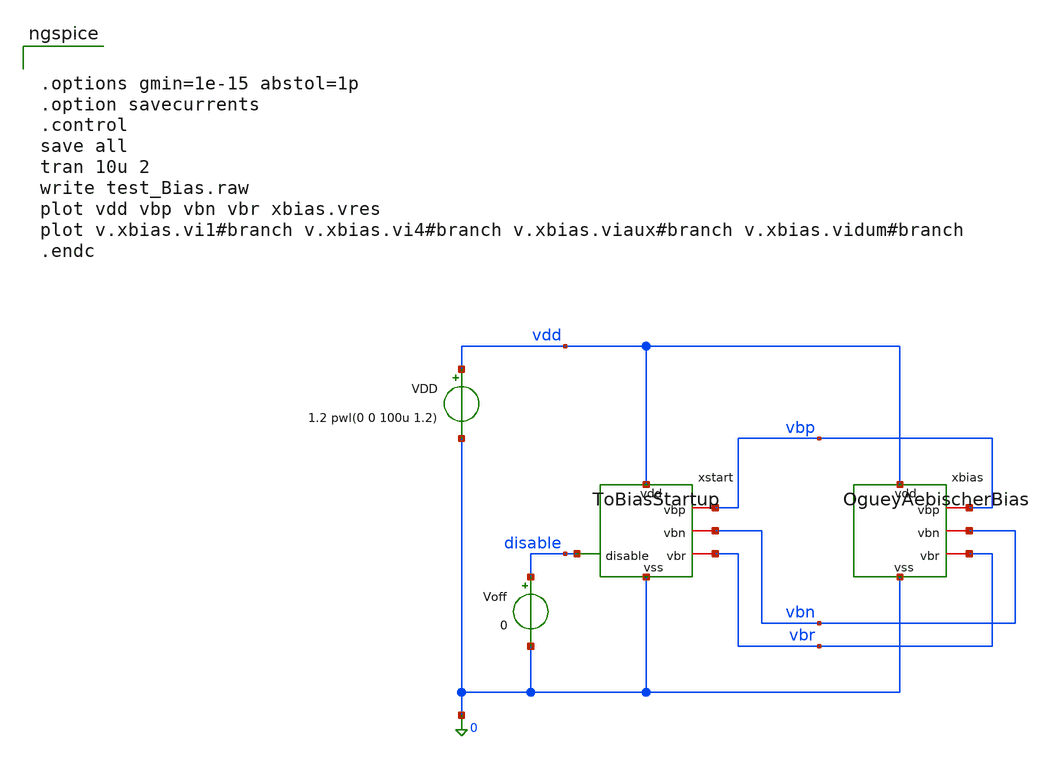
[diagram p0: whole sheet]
** sch_path: playground/test_Bias.sch
**.subckt test_Bias
xbias vdd vbp vbn vbr 0 OgueyAebischerBias
xstart vdd vbp vbn disable vbr 0 ToBiasStartup
VDD vdd 0 1.2 pwl(0 0 100u 1.2)
Voff disable 0 0
**** begin user architecture code


.options gmin=1e-15 abstol=1p
.option savecurrents
.control
save all
tran 10u 2
write test_Bias.raw
plot vdd vbp vbn vbr xbias.vres
plot v.xbias.vi1#branch v.xbias.vi4#branch v.xbias.viaux#branch v.xbias.vidum#branch
.endc


 .lib $::SKYWATER_MODELS/models/sky130.lib.spice tt

.param mc_mm_switch=0
.param mc_pr_switch=1


**** end user architecture code
**.ends

* expanding   symbol:  OgueyAebischerBias.sym # of pins=5
** sym_path: OgueyAebischerBias.sym
** sch_path: OgueyAebischerBias.sch
.subckt OgueyAebischerBias vdd vbp vbn vbr vss
*.iopin vss
*.iopin vdd
*.iopin vbp
*.iopin vbn
*.iopin vbr
XM10 net3 vbn vres vss sky130_fd_pr__nfet_01v8 L=10 W=1 nf=1 ad='int((1 + 1)/2) * 1 / 1 * 0.29' as='int((1 + 2)/2) * 1 / 1 * 0.29'
+ pd='2*int((1 + 1)/2) * (1 / 1 + 0.29)' ps='2*int((1 + 2)/2) * (1 / 1 + 0.29)' nrd='0.29 / 1 ' nrs='0.29 / 1 '
+ sa=0 sb=0 sd=0 mult=4 m=4
XM12 vbp vbp vdd vdd sky130_fd_pr__pfet_01v8 L=10 W=1 nf=1 ad='int((nf+1)/2) * W/nf * 0.29' as='int((nf+2)/2) * W/nf * 0.29'
+ pd='2*int((nf+1)/2) * (W/nf + 0.29)' ps='2*int((nf+2)/2) * (W/nf + 0.29)' nrd='0.29 / W' nrs='0.29 / W'
+ sa=0 sb=0 sd=0 mult=1 m=1
XM11 vbn vbn vss vss sky130_fd_pr__nfet_01v8 L=10 W=1 nf=1 ad='int((1 + 1)/2) * 1 / 1 * 0.29' as='int((1 + 2)/2) * 1 / 1 * 0.29'
+ pd='2*int((1 + 1)/2) * (1 / 1 + 0.29)' ps='2*int((1 + 2)/2) * (1 / 1 + 0.29)' nrd='0.29 / 1 ' nrs='0.29 / 1 '
+ sa=0 sb=0 sd=0 mult=1 m=1
XM13 net2 vbp vdd vdd sky130_fd_pr__pfet_01v8 L=10 W=1 nf=1 ad='int((nf+1)/2) * W/nf * 0.29' as='int((nf+2)/2) * W/nf * 0.29'
+ pd='2*int((nf+1)/2) * (W/nf + 0.29)' ps='2*int((nf+2)/2) * (W/nf + 0.29)' nrd='0.29 / W' nrs='0.29 / W'
+ sa=0 sb=0 sd=0 mult=4 m=4
XM14 net1 vbp vdd vdd sky130_fd_pr__pfet_01v8 L=10 W=1 nf=1 ad='int((nf+1)/2) * W/nf * 0.29' as='int((nf+2)/2) * W/nf * 0.29'
+ pd='2*int((nf+1)/2) * (W/nf + 0.29)' ps='2*int((nf+2)/2) * (W/nf + 0.29)' nrd='0.29 / W' nrs='0.29 / W'
+ sa=0 sb=0 sd=0 mult=1 m=1
XM16 net4 vbr vss vss sky130_fd_pr__nfet_01v8 L=80 W=0.5 nf=1 ad='int((1 + 1)/2) * 0.5 / 1 * 0.29' as='int((1 + 2)/2) * 0.5 / 1 * 0.29'
+ pd='2*int((1 + 1)/2) * (0.5 / 1 + 0.29)' ps='2*int((1 + 2)/2) * (0.5 / 1 + 0.29)' nrd='0.29 / 0.5 ' nrs='0.29 / 0.5 '
+ sa=0 sb=0 sd=0 mult=1 m=1
XM15 vbr vbr vss vss sky130_fd_pr__nfet_01v8 L=80 W=0.5 nf=1 ad='int((1 + 1)/2) * 0.5 / 1 * 0.29' as='int((1 + 2)/2) * 0.5 / 1 * 0.29'
+ pd='2*int((1 + 1)/2) * (0.5 / 1 + 0.29)' ps='2*int((1 + 2)/2) * (0.5 / 1 + 0.29)' nrd='0.29 / 0.5 ' nrs='0.29 / 0.5 '
+ sa=0 sb=0 sd=0 mult=1 m=1
Vi1 vbp net3 0
.save i(vi1)
Vi4 net2 vbn 0
.save i(vi4)
Viaux net1 vbr 0
.save i(viaux)
R1 vres vss 10000k m=1
Vidum net5 net4 0
.save i(vidum)
E1 vdd net5 vdd vres 1
.ends


* expanding   symbol:  ToBiasStartup.sym # of pins=6
** sym_path: ToBiasStartup.sym
** sch_path: ToBiasStartup.sch
.subckt ToBiasStartup vdd vbp vbn disable vbr vss
*.iopin vss
*.iopin vdd
*.iopin vbp
*.iopin vbn
*.iopin vbr
*.ipin disable
XM24 vbr disable vss vss sky130_fd_pr__nfet_01v8 L=0.3 W=1 nf=1 ad='int((1 + 1)/2) * 1 / 1 * 0.29' as='int((1 + 2)/2) * 1 / 1 * 0.29'
+ pd='2*int((1 + 1)/2) * (1 / 1 + 0.29)' ps='2*int((1 + 2)/2) * (1 / 1 + 0.29)' nrd='0.29 / 1 ' nrs='0.29 / 1 '
+ sa=0 sb=0 sd=0 mult=1 m=1
XM22 vbr vkick vdd vdd sky130_fd_pr__pfet_01v8 L=0.3 W=1 nf=1 ad='int((nf+1)/2) * W/nf * 0.29' as='int((nf+2)/2) * W/nf * 0.29'
+ pd='2*int((nf+1)/2) * (W/nf + 0.29)' ps='2*int((nf+2)/2) * (W/nf + 0.29)' nrd='0.29 / W' nrs='0.29 / W'
+ sa=0 sb=0 sd=0 mult=1 m=1
XM25 vkick vbp vdd vdd sky130_fd_pr__pfet_01v8 L=0.3 W=1 nf=1 ad='int((nf+1)/2) * W/nf * 0.29' as='int((nf+2)/2) * W/nf * 0.29'
+ pd='2*int((nf+1)/2) * (W/nf + 0.29)' ps='2*int((nf+2)/2) * (W/nf + 0.29)' nrd='0.29 / W' nrs='0.29 / W'
+ sa=0 sb=0 sd=0 mult=1 m=1
XM23 vbn disable vss vss sky130_fd_pr__nfet_01v8 L=0.3 W=1 nf=1 ad='int((1 + 1)/2) * 1 / 1 * 0.29' as='int((1 + 2)/2) * 1 / 1 * 0.29'
+ pd='2*int((1 + 1)/2) * (1 / 1 + 0.29)' ps='2*int((1 + 2)/2) * (1 / 1 + 0.29)' nrd='0.29 / 1 ' nrs='0.29 / 1 '
+ sa=0 sb=0 sd=0 mult=1 m=1
XM21 vbn vkick vdd vdd sky130_fd_pr__pfet_01v8 L=0.3 W=1 nf=1 ad='int((nf+1)/2) * W/nf * 0.29' as='int((nf+2)/2) * W/nf * 0.29'
+ pd='2*int((nf+1)/2) * (W/nf + 0.29)' ps='2*int((nf+2)/2) * (W/nf + 0.29)' nrd='0.29 / W' nrs='0.29 / W'
+ sa=0 sb=0 sd=0 mult=1 m=1
XM20 disable vkick disable vss sky130_fd_pr__nfet_01v8 L=4 W=4 nf=1 ad='int((1 + 1)/2) * 4 / 1 * 0.29'
+ as='int((1 + 2)/2) * 4 / 1 * 0.29' pd='2*int((1 + 1)/2) * (4 / 1 + 0.29)' ps='2*int((1 + 2)/2) * (4 / 1 + 0.29)'
+ nrd='0.29 / 4 ' nrs='0.29 / 4 ' sa=0 sb=0 sd=0 mult=1 m=1
XM26 vdd vbp vdd vss sky130_fd_pr__nfet_01v8 L=4 W=4 nf=1 ad='int((1 + 1)/2) * 4 / 1 * 0.29' as='int((1 + 2)/2) * 4 / 1 * 0.29'
+ pd='2*int((1 + 1)/2) * (4 / 1 + 0.29)' ps='2*int((1 + 2)/2) * (4 / 1 + 0.29)' nrd='0.29 / 4 ' nrs='0.29 / 4 '
+ sa=0 sb=0 sd=0 mult=1 m=1
.ends

.end
